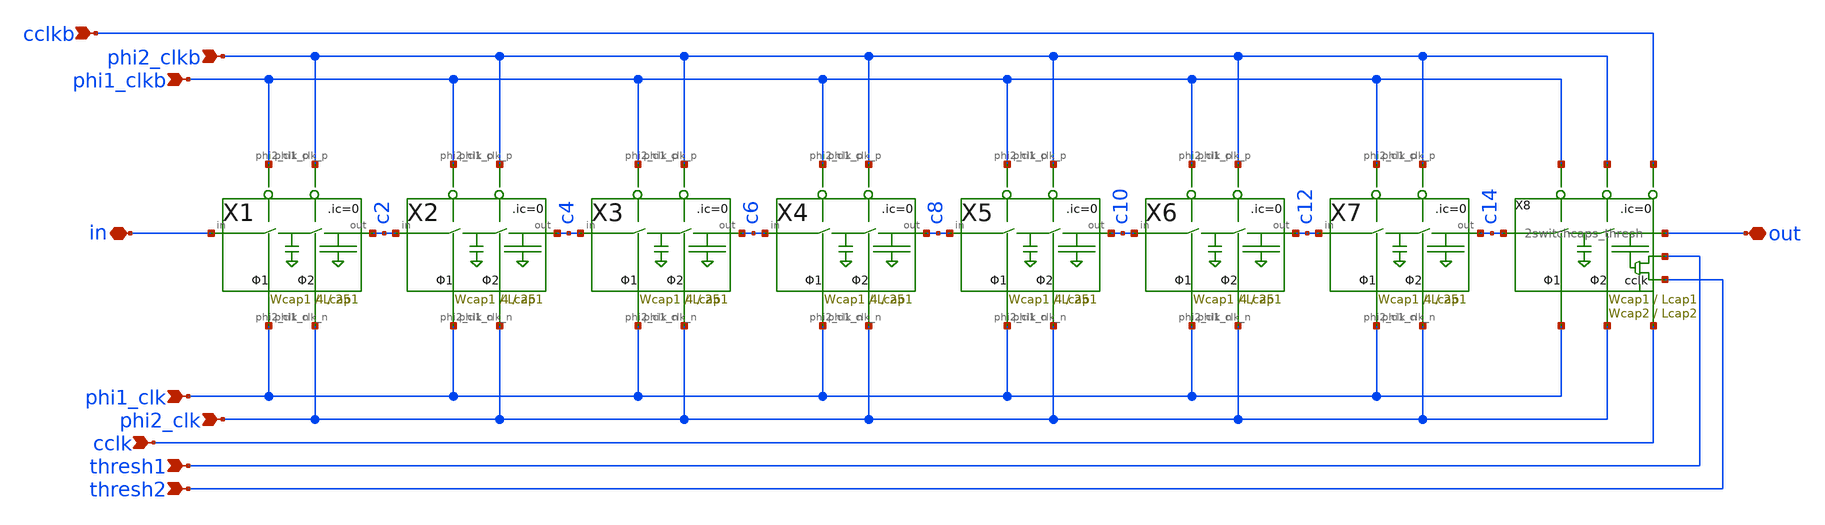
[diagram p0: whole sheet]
** sch_path: xschem/Switched_Caps/16switchcaps_2phi_thresh.sch
**.subckt 16switchcaps_2phi_thresh in out phi2_clkb phi1_clkb phi2_clk phi1_clk thresh1 cclk thresh2
*+ cclkb
*.iopin in
*.iopin out
*.ipin phi2_clkb
*.ipin phi1_clkb
*.ipin phi2_clk
*.ipin phi1_clk
*.ipin thresh1
*.ipin cclk
*.ipin thresh2
*.ipin cclkb
X1 in c2 phi2_clk phi1_clk phi1_clkb phi2_clkb 2switchcaps Wcap1=Wcap1 Lcap1=Lcap1 Wcap2=4 Lcap2=25
X2 c2 c4 phi2_clk phi1_clk phi1_clkb phi2_clkb 2switchcaps Wcap1=Wcap1 Lcap1=Lcap1 Wcap2=4 Lcap2=25
X3 c4 c6 phi2_clk phi1_clk phi1_clkb phi2_clkb 2switchcaps Wcap1=Wcap1 Lcap1=Lcap1 Wcap2=4 Lcap2=25
X4 c6 c8 phi2_clk phi1_clk phi1_clkb phi2_clkb 2switchcaps Wcap1=Wcap1 Lcap1=Lcap1 Wcap2=4 Lcap2=25
X5 c8 c10 phi2_clk phi1_clk phi1_clkb phi2_clkb 2switchcaps Wcap1=Wcap1 Lcap1=Lcap1 Wcap2=4 Lcap2=25
X6 c10 c12 phi2_clk phi1_clk phi1_clkb phi2_clkb 2switchcaps Wcap1=Wcap1 Lcap1=Lcap1 Wcap2=4
+ Lcap2=25
X7 c12 c14 phi2_clk phi1_clk phi1_clkb phi2_clkb 2switchcaps Wcap1=Wcap1 Lcap1=Lcap1 Wcap2=4
+ Lcap2=25
X8 c14 out phi2_clk phi1_clk phi1_clkb phi2_clkb thresh2 cclk thresh1 cclkb 2switchcaps_thresh
+ Wcap1=Wcap1 Lcap1=Lcap1 Wcap2=Wcap2 Lcap2=Lcap2
**.ends

* expanding   symbol:  Switched_Caps/2switchcaps.sym # of pins=6
** sym_path: xschem/Switched_Caps/2switchcaps.sym
** sch_path: xschem/Switched_Caps/2switchcaps.sch
.subckt 2switchcaps in out phi2_clk_n phi1_clk_n phi1_clk_p phi2_clk_p  Wcap1=4 Lcap1=2.5 Wcap2=4
+ Lcap2=25
*.iopin out
*.iopin in
*.ipin phi1_clk_n
*.ipin phi1_clk_p
*.ipin phi2_clk_p
*.ipin phi2_clk_n
XC1 c1 GND sky130_fd_pr__cap_mim_m3_1 W=Wcap1 L=Lcap1 MF=1 m=1
XC2 out GND sky130_fd_pr__cap_mim_m3_1 W=Wcap2 L=Lcap2 MF=1 m=1
**** begin user architecture code

.ic v(c1)=0 v(out)=0

**** end user architecture code
X1 in c1 phi1_clk_p phi1_clk_n transmission_gate Wpmos=0.42 Lpmos=0.18 Wnmos=0.42 Lnmos=0.18
X2 c1 out phi2_clk_p phi2_clk_n transmission_gate Wpmos=0.42 Lpmos=0.18 Wnmos=0.42 Lnmos=0.18
.ends


* expanding   symbol:  Switched_Caps/2switchcaps_thresh.sym # of pins=10
** sym_path: xschem/Switched_Caps/2switchcaps_thresh.sym
** sch_path: xschem/Switched_Caps/2switchcaps_thresh.sch
.subckt 2switchcaps_thresh in out phi2_clk_n phi1_clk_n phi1_clk_p phi2_clk_p thresh2 cclk thresh1
+ cclkb  Wcap1=4 Lcap1=2.5 Wcap2=4 Lcap2=25
*.iopin out
*.iopin in
*.ipin phi1_clk_n
*.ipin phi1_clk_p
*.ipin phi2_clk_p
*.ipin phi2_clk_n
*.ipin thresh1
*.ipin cclk
*.ipin thresh2
*.ipin cclkb
XC1 c1 GND sky130_fd_pr__cap_mim_m3_1 W=Wcap1 L=Lcap1 MF=1 m=1
XC2 out c2b sky130_fd_pr__cap_mim_m3_1 W=Wcap2 L=Lcap2 MF=1 m=1
**** begin user architecture code


*init cap top and bottom plates at 0V:
.ic v(c1)=0 v(out)=0
*c2 will settle at thresh1
*.ic v(xc1.a)=0 v(xc1.b1)=0 v(xc2.a)=0 v(xc2.b1)=0


**** end user architecture code
X1 in c1 phi1_clk_p phi1_clk_n transmission_gate Wpmos=0.42 Lpmos=0.18 Wnmos=0.42 Lnmos=0.18
X2 c1 out phi2_clk_p phi2_clk_n transmission_gate Wpmos=0.42 Lpmos=0.18 Wnmos=0.42 Lnmos=0.18
x3 thresh2 thresh1 cclk cclkb c2b analogMux
.ends


* expanding   symbol:  transmission_gate/transmission_gate.sym # of pins=4
** sym_path: xschem/transmission_gate/transmission_gate.sym
** sch_path: xschem/transmission_gate/transmission_gate.sch
.subckt transmission_gate in out ctrl_ ctrl  Wpmos=0.42 Lpmos=0.18 Wnmos=0.42 Lnmos=0.18
*.iopin in
*.iopin out
*.ipin ctrl_
*.ipin ctrl
XM1 out ctrl in GND sky130_fd_pr__nfet_01v8 L=Lnmos W=Wnmos nf=1 ad='int((nf+1)/2) * W/nf * 0.29' as='int((nf+2)/2) * W/nf * 0.29'
+ pd='2*int((nf+1)/2) * (W/nf + 0.29)' ps='2*int((nf+2)/2) * (W/nf + 0.29)' nrd='0.29 / W' nrs='0.29 / W'
+ sa=0 sb=0 sd=0 mult=1 m=1
XM2 out ctrl_ in VDD sky130_fd_pr__pfet_01v8 L=Lpmos W=Wpmos nf=1 ad='int((nf+1)/2) * W/nf * 0.29' as='int((nf+2)/2) * W/nf * 0.29'
+ pd='2*int((nf+1)/2) * (W/nf + 0.29)' ps='2*int((nf+2)/2) * (W/nf + 0.29)' nrd='0.29 / W' nrs='0.29 / W'
+ sa=0 sb=0 sd=0 mult=1 m=1
.ends


* expanding   symbol:  comparator/analogMux.sym # of pins=5
** sym_path: xschem/comparator/analogMux.sym
** sch_path: xschem/comparator/analogMux.sch
.subckt analogMux Vref2 Vref1 C Cbar out
*.ipin Vref1
*.opin out
*.ipin Vref2
*.ipin C
*.ipin Cbar
XM1 Vref1 C out GND sky130_fd_pr__nfet_01v8 L=1 W=4 nf=1 ad='int((nf+1)/2) * W/nf * 0.29' as='int((nf+2)/2) * W/nf * 0.29'
+ pd='2*int((nf+1)/2) * (W/nf + 0.29)' ps='2*int((nf+2)/2) * (W/nf + 0.29)' nrd='0.29 / W' nrs='0.29 / W'
+ sa=0 sb=0 sd=0 mult=1 m=1
XM2 Vref1 Cbar out VDD sky130_fd_pr__pfet_01v8 L=1 W=8 nf=1 ad='int((nf+1)/2) * W/nf * 0.29' as='int((nf+2)/2) * W/nf * 0.29'
+ pd='2*int((nf+1)/2) * (W/nf + 0.29)' ps='2*int((nf+2)/2) * (W/nf + 0.29)' nrd='0.29 / W' nrs='0.29 / W'
+ sa=0 sb=0 sd=0 mult=1 m=1
XM3 out Cbar Vref2 GND sky130_fd_pr__nfet_01v8 L=1 W=4 nf=1 ad='int((nf+1)/2) * W/nf * 0.29' as='int((nf+2)/2) * W/nf * 0.29'
+ pd='2*int((nf+1)/2) * (W/nf + 0.29)' ps='2*int((nf+2)/2) * (W/nf + 0.29)' nrd='0.29 / W' nrs='0.29 / W'
+ sa=0 sb=0 sd=0 mult=1 m=1
XM4 out C Vref2 VDD sky130_fd_pr__pfet_01v8 L=1 W=8 nf=1 ad='int((nf+1)/2) * W/nf * 0.29' as='int((nf+2)/2) * W/nf * 0.29'
+ pd='2*int((nf+1)/2) * (W/nf + 0.29)' ps='2*int((nf+2)/2) * (W/nf + 0.29)' nrd='0.29 / W' nrs='0.29 / W'
+ sa=0 sb=0 sd=0 mult=1 m=1
.ends

.GLOBAL GND
.GLOBAL VDD
.end
